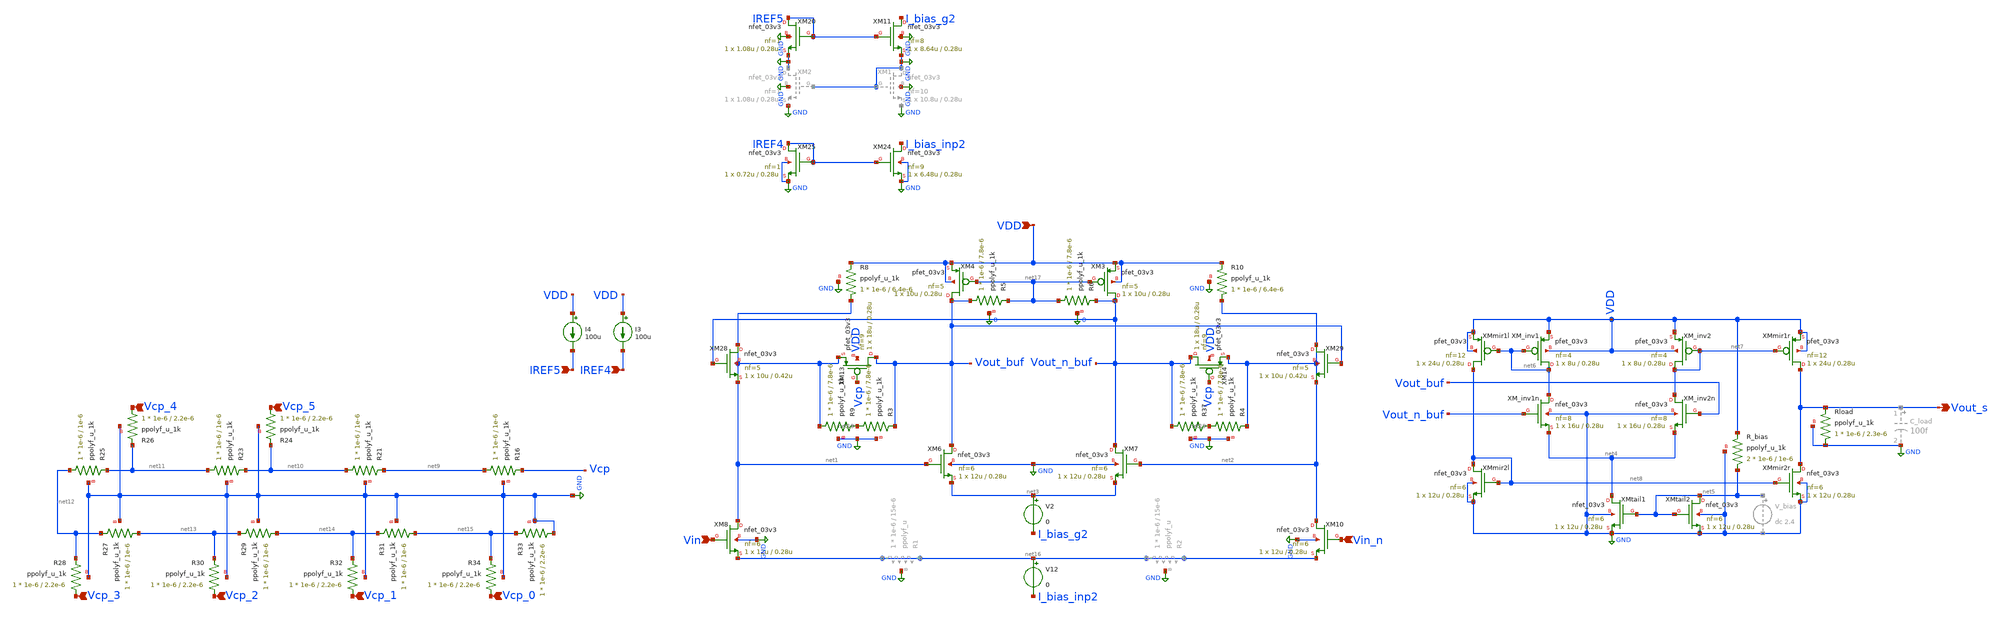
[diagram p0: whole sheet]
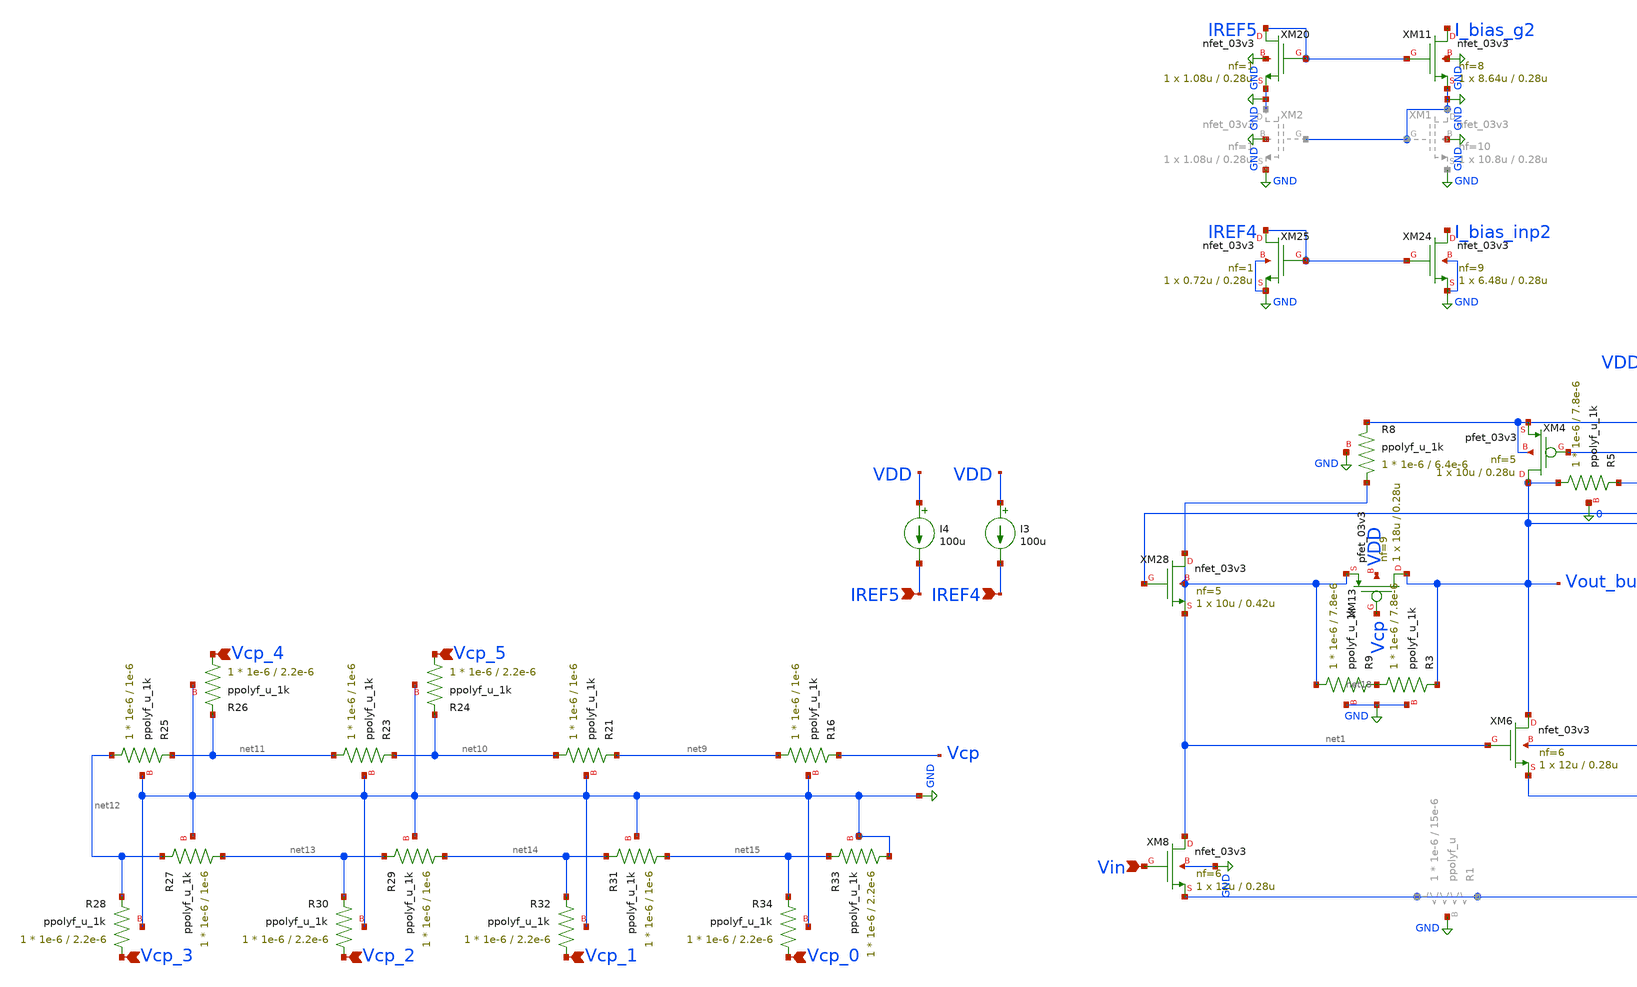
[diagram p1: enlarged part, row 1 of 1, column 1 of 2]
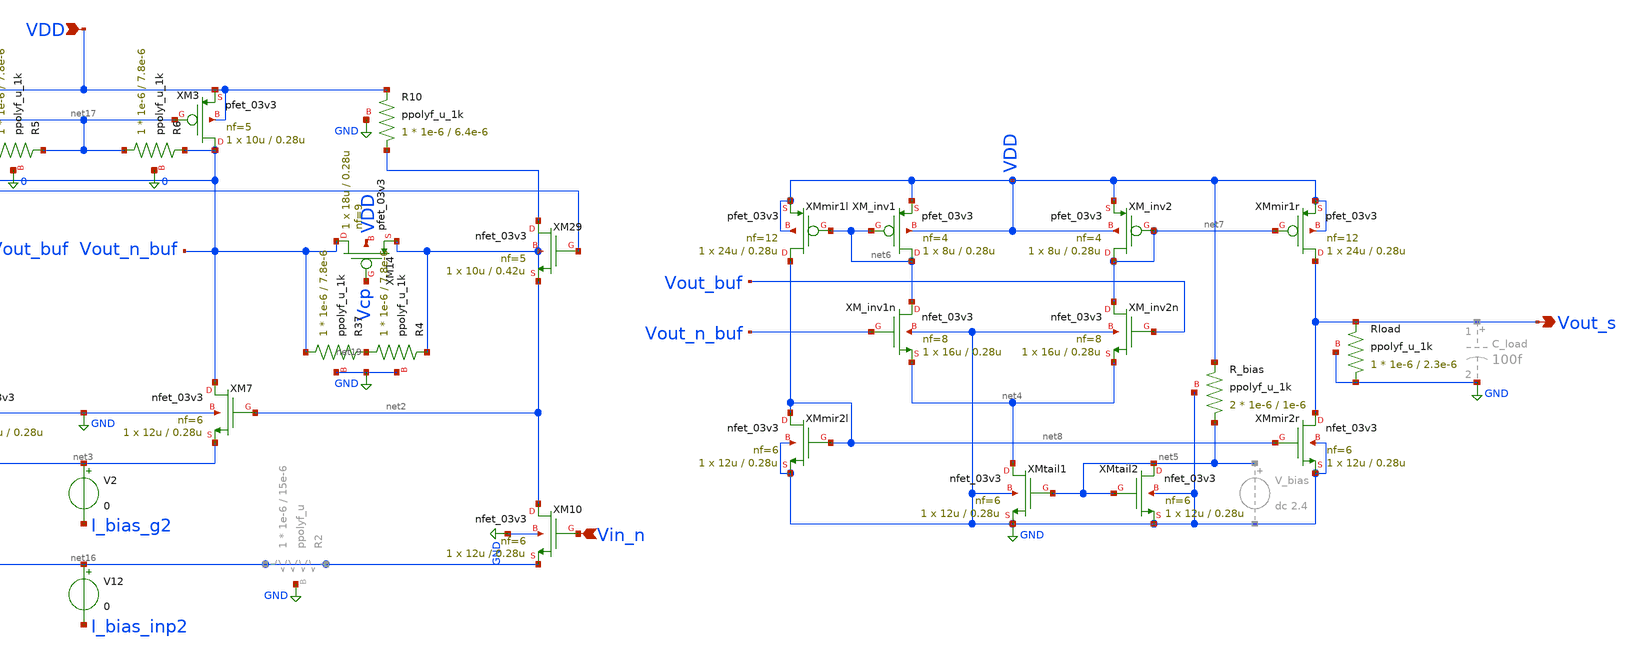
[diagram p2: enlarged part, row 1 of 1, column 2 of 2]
** sch_path: blocks/adc/vga/vga.sch
**.subckt vga VDD Vin_n Vin Vout_s Vcp_0 Vcp_1 Vcp_2 Vcp_3 Vcp_4 Vcp_5 IREF4 IREF5
*.ipin VDD
*.ipin Vin_n
*.ipin Vin
*.opin Vout_s
*.ipin Vcp_0
*.ipin Vcp_1
*.ipin Vcp_2
*.ipin Vcp_3
*.ipin Vcp_4
*.ipin Vcp_5
*.ipin IREF4
*.ipin IREF5
XM6 Vout_buf net1 net3 GND nfet_03v3 L=0.28u W=12u nf=6 ad='int((nf+1)/2) * W/nf * 0.18u' as='int((nf+2)/2) * W/nf * 0.18u'
+ pd='2*int((nf+1)/2) * (W/nf + 0.18u)' ps='2*int((nf+2)/2) * (W/nf + 0.18u)' nrd='0.18u / W' nrs='0.18u / W'
+ sa=0 sb=0 sd=0 m=1
XM7 Vout_n_buf net2 net3 GND nfet_03v3 L=0.28u W=12u nf=6 ad='int((nf+1)/2) * W/nf * 0.18u' as='int((nf+2)/2) * W/nf * 0.18u'
+ pd='2*int((nf+1)/2) * (W/nf + 0.18u)' ps='2*int((nf+2)/2) * (W/nf + 0.18u)' nrd='0.18u / W' nrs='0.18u / W'
+ sa=0 sb=0 sd=0 m=1
XM8 net1 Vin net16 GND nfet_03v3 L=0.28u W=12u nf=6 ad='int((nf+1)/2) * W/nf * 0.18u' as='int((nf+2)/2) * W/nf * 0.18u'
+ pd='2*int((nf+1)/2) * (W/nf + 0.18u)' ps='2*int((nf+2)/2) * (W/nf + 0.18u)' nrd='0.18u / W' nrs='0.18u / W'
+ sa=0 sb=0 sd=0 m=1
XM10 net2 Vin_n net16 GND nfet_03v3 L=0.28u W=12u nf=6 ad='int((nf+1)/2) * W/nf * 0.18u' as='int((nf+2)/2) * W/nf * 0.18u'
+ pd='2*int((nf+1)/2) * (W/nf + 0.18u)' ps='2*int((nf+2)/2) * (W/nf + 0.18u)' nrd='0.18u / W' nrs='0.18u / W'
+ sa=0 sb=0 sd=0 m=1
XM28 net1 Vout_n_buf net1 net1 nfet_03v3 L=0.42u W=10u nf=5 ad='int((nf+1)/2) * W/nf * 0.18u' as='int((nf+2)/2) * W/nf * 0.18u'
+ pd='2*int((nf+1)/2) * (W/nf + 0.18u)' ps='2*int((nf+2)/2) * (W/nf + 0.18u)' nrd='0.18u / W' nrs='0.18u / W'
+ sa=0 sb=0 sd=0 m=1
XM29 net2 Vout_buf net2 net2 nfet_03v3 L=0.42u W=10u nf=5 ad='int((nf+1)/2) * W/nf * 0.18u' as='int((nf+2)/2) * W/nf * 0.18u'
+ pd='2*int((nf+1)/2) * (W/nf + 0.18u)' ps='2*int((nf+2)/2) * (W/nf + 0.18u)' nrd='0.18u / W' nrs='0.18u / W'
+ sa=0 sb=0 sd=0 m=1
XM_inv1 net6 net6 VDD VDD pfet_03v3 L=0.28u W=8u nf=4 ad='int((nf+1)/2) * W/nf * 0.18u' as='int((nf+2)/2) * W/nf * 0.18u'
+ pd='2*int((nf+1)/2) * (W/nf + 0.18u)' ps='2*int((nf+2)/2) * (W/nf + 0.18u)' nrd='0.18u / W' nrs='0.18u / W'
+ sa=0 sb=0 sd=0 m=1
XM_inv1n net6 Vout_n_buf net4 GND nfet_03v3 L=0.28u W=16u nf=8 ad='int((nf+1)/2) * W/nf * 0.18u' as='int((nf+2)/2) * W/nf * 0.18u'
+ pd='2*int((nf+1)/2) * (W/nf + 0.18u)' ps='2*int((nf+2)/2) * (W/nf + 0.18u)' nrd='0.18u / W' nrs='0.18u / W'
+ sa=0 sb=0 sd=0 m=1
XM_inv2 net7 net7 VDD VDD pfet_03v3 L=0.28u W=8u nf=4 ad='int((nf+1)/2) * W/nf * 0.18u' as='int((nf+2)/2) * W/nf * 0.18u'
+ pd='2*int((nf+1)/2) * (W/nf + 0.18u)' ps='2*int((nf+2)/2) * (W/nf + 0.18u)' nrd='0.18u / W' nrs='0.18u / W'
+ sa=0 sb=0 sd=0 m=1
XM_inv2n net7 Vout_buf net4 GND nfet_03v3 L=0.28u W=16u nf=8 ad='int((nf+1)/2) * W/nf * 0.18u' as='int((nf+2)/2) * W/nf * 0.18u'
+ pd='2*int((nf+1)/2) * (W/nf + 0.18u)' ps='2*int((nf+2)/2) * (W/nf + 0.18u)' nrd='0.18u / W' nrs='0.18u / W'
+ sa=0 sb=0 sd=0 m=1
XMtail1 net4 net5 GND GND nfet_03v3 L=0.28u W=12u nf=6 ad='int((nf+1)/2) * W/nf * 0.18u' as='int((nf+2)/2) * W/nf * 0.18u'
+ pd='2*int((nf+1)/2) * (W/nf + 0.18u)' ps='2*int((nf+2)/2) * (W/nf + 0.18u)' nrd='0.18u / W' nrs='0.18u / W'
+ sa=0 sb=0 sd=0 m=1
XMtail2 net5 net5 GND GND nfet_03v3 L=0.28u W=12u nf=6 ad='int((nf+1)/2) * W/nf * 0.18u' as='int((nf+2)/2) * W/nf * 0.18u'
+ pd='2*int((nf+1)/2) * (W/nf + 0.18u)' ps='2*int((nf+2)/2) * (W/nf + 0.18u)' nrd='0.18u / W' nrs='0.18u / W'
+ sa=0 sb=0 sd=0 m=1
XMmir1l net8 net6 VDD VDD pfet_03v3 L=0.28u W=24u nf=12 ad='int((nf+1)/2) * W/nf * 0.18u' as='int((nf+2)/2) * W/nf * 0.18u'
+ pd='2*int((nf+1)/2) * (W/nf + 0.18u)' ps='2*int((nf+2)/2) * (W/nf + 0.18u)' nrd='0.18u / W' nrs='0.18u / W'
+ sa=0 sb=0 sd=0 m=1
XMmir1r Vout_s net7 VDD VDD pfet_03v3 L=0.28u W=24u nf=12 ad='int((nf+1)/2) * W/nf * 0.18u' as='int((nf+2)/2) * W/nf * 0.18u'
+ pd='2*int((nf+1)/2) * (W/nf + 0.18u)' ps='2*int((nf+2)/2) * (W/nf + 0.18u)' nrd='0.18u / W' nrs='0.18u / W'
+ sa=0 sb=0 sd=0 m=1
XMmir2l net8 net8 GND GND nfet_03v3 L=0.28u W=12u nf=6 ad='int((nf+1)/2) * W/nf * 0.18u' as='int((nf+2)/2) * W/nf * 0.18u'
+ pd='2*int((nf+1)/2) * (W/nf + 0.18u)' ps='2*int((nf+2)/2) * (W/nf + 0.18u)' nrd='0.18u / W' nrs='0.18u / W'
+ sa=0 sb=0 sd=0 m=1
XMmir2r Vout_s net8 GND GND nfet_03v3 L=0.28u W=12u nf=6 ad='int((nf+1)/2) * W/nf * 0.18u' as='int((nf+2)/2) * W/nf * 0.18u'
+ pd='2*int((nf+1)/2) * (W/nf + 0.18u)' ps='2*int((nf+2)/2) * (W/nf + 0.18u)' nrd='0.18u / W' nrs='0.18u / W'
+ sa=0 sb=0 sd=0 m=1
XR_bias net5 VDD GND ppolyf_u_1k r_width=1e-6 r_length=1e-6 m=2
XR16 net9 Vcp GND ppolyf_u_1k r_width=1e-6 r_length=1e-6 m=1
XR21 net10 net9 GND ppolyf_u_1k r_width=1e-6 r_length=1e-6 m=1
XR23 net11 net10 GND ppolyf_u_1k r_width=1e-6 r_length=1e-6 m=1
XR24 Vcp_5 net10 GND ppolyf_u_1k r_width=1e-6 r_length=2.2e-6 m=1
XR25 net12 net11 GND ppolyf_u_1k r_width=1e-6 r_length=1e-6 m=1
XR26 Vcp_4 net11 GND ppolyf_u_1k r_width=1e-6 r_length=2.2e-6 m=1
XR27 net13 net12 GND ppolyf_u_1k r_width=1e-6 r_length=1e-6 m=1
XR28 Vcp_3 net12 GND ppolyf_u_1k r_width=1e-6 r_length=2.2e-6 m=1
XR29 net14 net13 GND ppolyf_u_1k r_width=1e-6 r_length=1e-6 m=1
XR30 Vcp_2 net13 GND ppolyf_u_1k r_width=1e-6 r_length=2.2e-6 m=1
XR31 net15 net14 GND ppolyf_u_1k r_width=1e-6 r_length=1e-6 m=1
XR32 Vcp_1 net14 GND ppolyf_u_1k r_width=1e-6 r_length=2.2e-6 m=1
XR33 GND net15 GND ppolyf_u_1k r_width=1e-6 r_length=2.2e-6 m=1
XR34 Vcp_0 net15 GND ppolyf_u_1k r_width=1e-6 r_length=2.2e-6 m=1
XM13 Vout_buf Vcp net1 VDD pfet_03v3 L=0.28u W=18u nf=9 ad='int((nf+1)/2) * W/nf * 0.18u' as='int((nf+2)/2) * W/nf * 0.18u'
+ pd='2*int((nf+1)/2) * (W/nf + 0.18u)' ps='2*int((nf+2)/2) * (W/nf + 0.18u)' nrd='0.18u / W' nrs='0.18u / W'
+ sa=0 sb=0 sd=0 m=1
XR9 net1 net18 GND ppolyf_u_1k r_width=1e-6 r_length=7.8e-6 m=1
XM14 Vout_n_buf Vcp net2 VDD pfet_03v3 L=0.28u W=18u nf=9 ad='int((nf+1)/2) * W/nf * 0.18u' as='int((nf+2)/2) * W/nf * 0.18u'
+ pd='2*int((nf+1)/2) * (W/nf + 0.18u)' ps='2*int((nf+2)/2) * (W/nf + 0.18u)' nrd='0.18u / W' nrs='0.18u / W'
+ sa=0 sb=0 sd=0 m=1
XR37 Vout_n_buf net19 GND ppolyf_u_1k r_width=1e-6 r_length=7.8e-6 m=1
XRload GND Vout_s GND ppolyf_u_1k r_width=1e-6 r_length=2.3e-6 m=1
XR8 net1 VDD GND ppolyf_u_1k r_width=1e-6 r_length=6.4e-6 m=1
XR10 net2 VDD GND ppolyf_u_1k r_width=1e-6 r_length=6.4e-6 m=1
XM11 I_bias_g2 IREF5 GND GND nfet_03v3 L=0.28u W=8.64u nf=8 ad='int((nf+1)/2) * W/nf * 0.18u' as='int((nf+2)/2) * W/nf * 0.18u'
+ pd='2*int((nf+1)/2) * (W/nf + 0.18u)' ps='2*int((nf+2)/2) * (W/nf + 0.18u)' nrd='0.18u / W' nrs='0.18u / W'
+ sa=0 sb=0 sd=0 m=1
XM20 IREF5 IREF5 GND GND nfet_03v3 L=0.28u W=1.08u nf=1 ad='int((nf+1)/2) * W/nf * 0.18u' as='int((nf+2)/2) * W/nf * 0.18u'
+ pd='2*int((nf+1)/2) * (W/nf + 0.18u)' ps='2*int((nf+2)/2) * (W/nf + 0.18u)' nrd='0.18u / W' nrs='0.18u / W'
+ sa=0 sb=0 sd=0 m=1
I3 VDD IREF4 100u
XM24 I_bias_inp2 IREF4 GND GND nfet_03v3 L=0.28u W=6.48u nf=9 ad='int((nf+1)/2) * W/nf * 0.18u' as='int((nf+2)/2) * W/nf * 0.18u'
+ pd='2*int((nf+1)/2) * (W/nf + 0.18u)' ps='2*int((nf+2)/2) * (W/nf + 0.18u)' nrd='0.18u / W' nrs='0.18u / W'
+ sa=0 sb=0 sd=0 m=1
XM25 IREF4 IREF4 GND GND nfet_03v3 L=0.28u W=0.72u nf=1 ad='int((nf+1)/2) * W/nf * 0.18u' as='int((nf+2)/2) * W/nf * 0.18u'
+ pd='2*int((nf+1)/2) * (W/nf + 0.18u)' ps='2*int((nf+2)/2) * (W/nf + 0.18u)' nrd='0.18u / W' nrs='0.18u / W'
+ sa=0 sb=0 sd=0 m=1
I4 VDD IREF5 100u
V12 net16 I_bias_inp2 0
XR3 net18 Vout_buf GND ppolyf_u_1k r_width=1e-6 r_length=7.8e-6 m=1
XR4 net19 net2 GND ppolyf_u_1k r_width=1e-6 r_length=7.8e-6 m=1
XM3 Vout_n_buf net17 VDD VDD pfet_03v3 L=0.28u W=10u nf=5 ad='int((nf+1)/2) * W/nf * 0.18u' as='int((nf+2)/2) * W/nf * 0.18u'
+ pd='2*int((nf+1)/2) * (W/nf + 0.18u)' ps='2*int((nf+2)/2) * (W/nf + 0.18u)' nrd='0.18u / W' nrs='0.18u / W'
+ sa=0 sb=0 sd=0 m=1
XM4 Vout_buf net17 VDD VDD pfet_03v3 L=0.28u W=10u nf=5 ad='int((nf+1)/2) * W/nf * 0.18u' as='int((nf+2)/2) * W/nf * 0.18u'
+ pd='2*int((nf+1)/2) * (W/nf + 0.18u)' ps='2*int((nf+2)/2) * (W/nf + 0.18u)' nrd='0.18u / W' nrs='0.18u / W'
+ sa=0 sb=0 sd=0 m=1
XR5 Vout_buf net17 0 ppolyf_u_1k r_width=1e-6 r_length=7.8e-6 m=1
XR6 net17 Vout_n_buf 0 ppolyf_u_1k r_width=1e-6 r_length=7.8e-6 m=1
V2 net3 I_bias_g2 0
**.ends
.GLOBAL GND
.end
